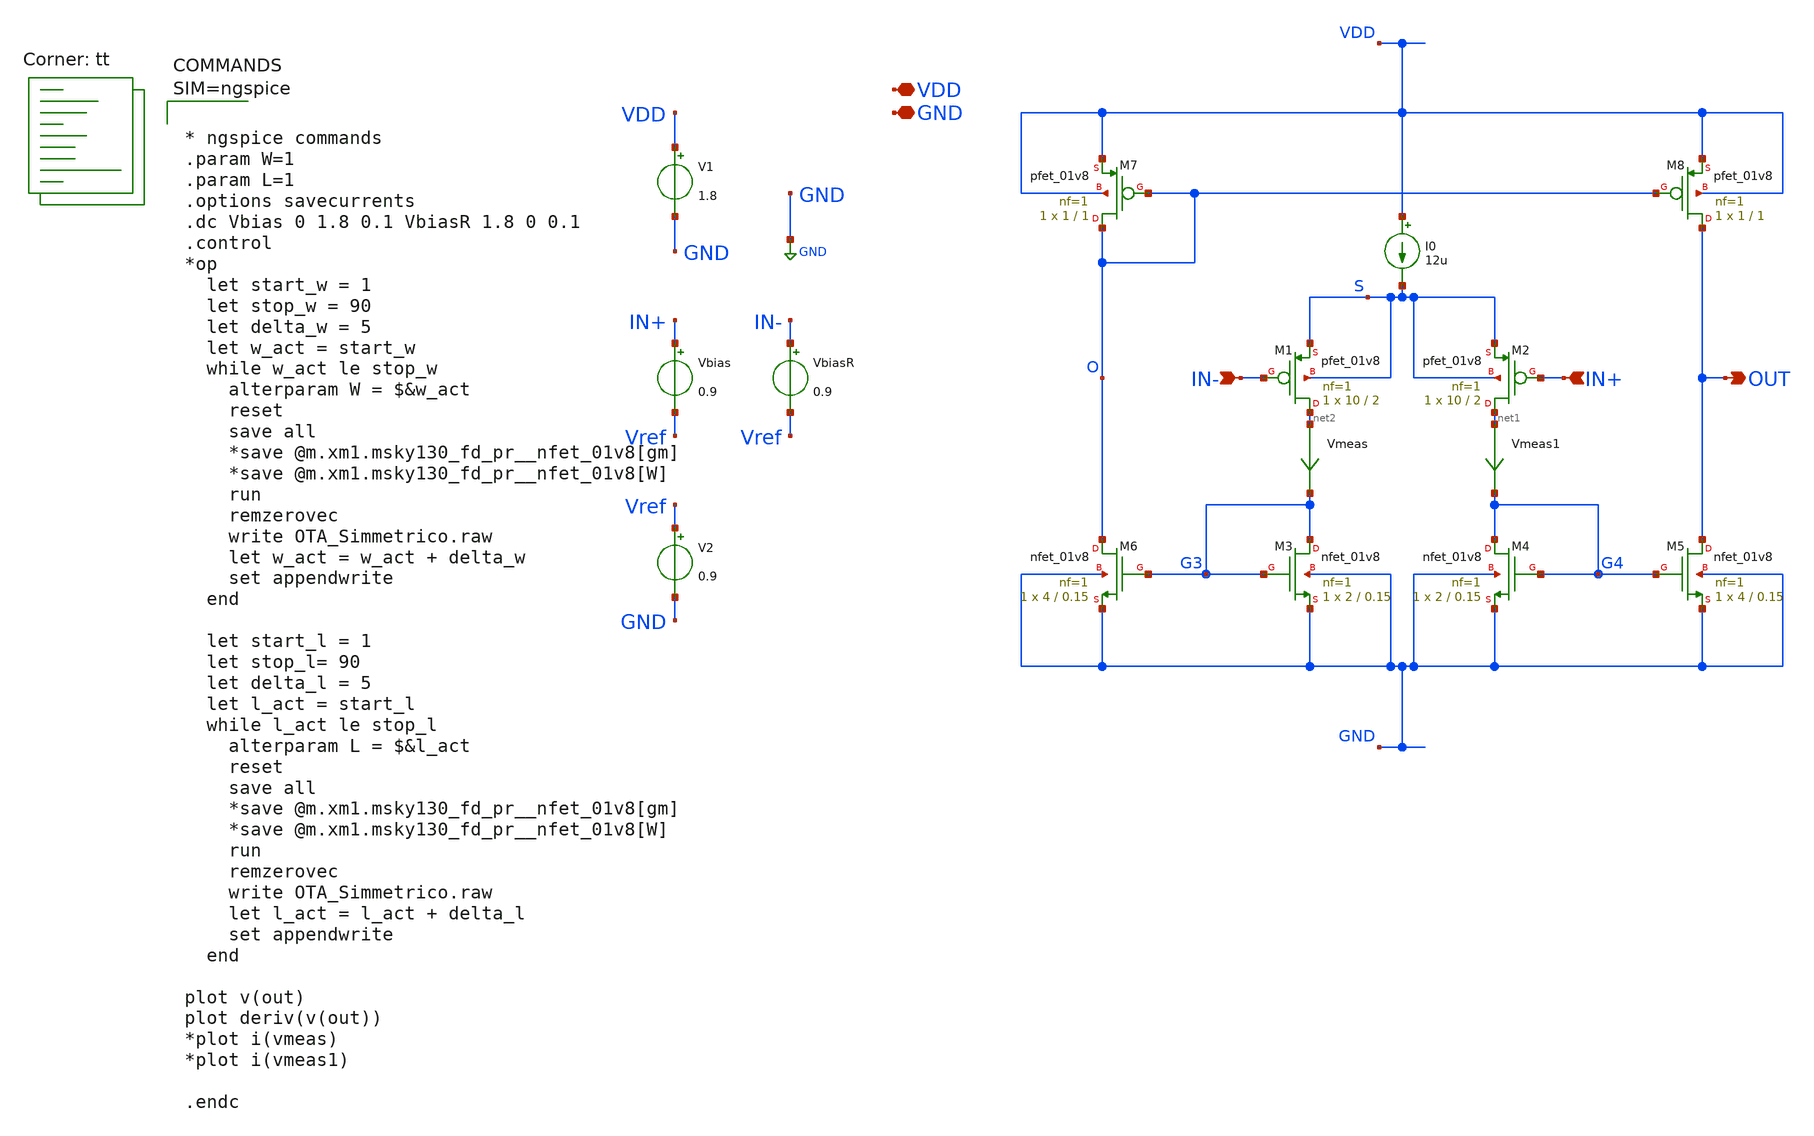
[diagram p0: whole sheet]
** sch_path: xschem/OTA_Simmetrico.sch
**.subckt OTA_Simmetrico VDD GND IN+ IN- OUT
*.iopin VDD
*.iopin GND
*.ipin IN+
*.ipin IN-
*.opin OUT
XM1 net2 IN- S S sky130_fd_pr__pfet_01v8 L=2 W=10 nf=1 ad='int((nf+1)/2) * W/nf * 0.29' as='int((nf+2)/2) * W/nf * 0.29'
+ pd='2*int((nf+1)/2) * (W/nf + 0.29)' ps='2*int((nf+2)/2) * (W/nf + 0.29)' nrd='0.29 / W' nrs='0.29 / W'
+ sa=0 sb=0 sd=0 mult=1 m=1
XM2 net1 IN+ S S sky130_fd_pr__pfet_01v8 L=2 W=10 nf=1 ad='int((nf+1)/2) * W/nf * 0.29' as='int((nf+2)/2) * W/nf * 0.29'
+ pd='2*int((nf+1)/2) * (W/nf + 0.29)' ps='2*int((nf+2)/2) * (W/nf + 0.29)' nrd='0.29 / W' nrs='0.29 / W'
+ sa=0 sb=0 sd=0 mult=1 m=1
XM3 G3 G3 GND GND sky130_fd_pr__nfet_01v8 L=0.15 W=2 nf=1 ad='int((nf+1)/2) * W/nf * 0.29' as='int((nf+2)/2) * W/nf * 0.29'
+ pd='2*int((nf+1)/2) * (W/nf + 0.29)' ps='2*int((nf+2)/2) * (W/nf + 0.29)' nrd='0.29 / W' nrs='0.29 / W'
+ sa=0 sb=0 sd=0 mult=1 m=1
XM4 G4 G4 GND GND sky130_fd_pr__nfet_01v8 L=0.15 W=2 nf=1 ad='int((nf+1)/2) * W/nf * 0.29' as='int((nf+2)/2) * W/nf * 0.29'
+ pd='2*int((nf+1)/2) * (W/nf + 0.29)' ps='2*int((nf+2)/2) * (W/nf + 0.29)' nrd='0.29 / W' nrs='0.29 / W'
+ sa=0 sb=0 sd=0 mult=1 m=1
XM5 OUT G4 GND GND sky130_fd_pr__nfet_01v8 L=0.15 W=4 nf=1 ad='int((nf+1)/2) * W/nf * 0.29' as='int((nf+2)/2) * W/nf * 0.29'
+ pd='2*int((nf+1)/2) * (W/nf + 0.29)' ps='2*int((nf+2)/2) * (W/nf + 0.29)' nrd='0.29 / W' nrs='0.29 / W'
+ sa=0 sb=0 sd=0 mult=1 m=1
XM6 O G3 GND GND sky130_fd_pr__nfet_01v8 L=0.15 W=4 nf=1 ad='int((nf+1)/2) * W/nf * 0.29' as='int((nf+2)/2) * W/nf * 0.29'
+ pd='2*int((nf+1)/2) * (W/nf + 0.29)' ps='2*int((nf+2)/2) * (W/nf + 0.29)' nrd='0.29 / W' nrs='0.29 / W'
+ sa=0 sb=0 sd=0 mult=1 m=1
XM7 O O VDD VDD sky130_fd_pr__pfet_01v8 L=1 W=1 nf=1 ad='int((nf+1)/2) * W/nf * 0.29' as='int((nf+2)/2) * W/nf * 0.29'
+ pd='2*int((nf+1)/2) * (W/nf + 0.29)' ps='2*int((nf+2)/2) * (W/nf + 0.29)' nrd='0.29 / W' nrs='0.29 / W'
+ sa=0 sb=0 sd=0 mult=1 m=1
XM8 OUT O VDD VDD sky130_fd_pr__pfet_01v8 L=1 W=1 nf=1 ad='int((nf+1)/2) * W/nf * 0.29' as='int((nf+2)/2) * W/nf * 0.29'
+ pd='2*int((nf+1)/2) * (W/nf + 0.29)' ps='2*int((nf+2)/2) * (W/nf + 0.29)' nrd='0.29 / W' nrs='0.29 / W'
+ sa=0 sb=0 sd=0 mult=1 m=1
I0 VDD S 12u
V1 VDD GND 1.8
Vbias IN+ Vref 0.9
VbiasR IN- Vref 0.9
V2 Vref GND 0.9
Vmeas net2 G3 0
.save i(vmeas)
Vmeas1 net1 G4 0
.save i(vmeas1)
**** begin user architecture code



* ngspice commands
.param W=1
.param L=1
.options savecurrents
.dc Vbias 0 1.8 0.1 VbiasR 1.8 0 0.1
.control
*op
  let start_w = 1
  let stop_w = 90
  let delta_w = 5
  let w_act = start_w
  while w_act le stop_w
    alterparam W = $&w_act
    reset
    save all
    *save @m.xm1.msky130_fd_pr__nfet_01v8[gm]
    *save @m.xm1.msky130_fd_pr__nfet_01v8[W]
    run
    remzerovec
    write OTA_Simmetrico.raw
    let w_act = w_act + delta_w
    set appendwrite
  end

  let start_l = 1
  let stop_l= 90
  let delta_l = 5
  let l_act = start_l
  while l_act le stop_l
    alterparam L = $&l_act
    reset
    save all
    *save @m.xm1.msky130_fd_pr__nfet_01v8[gm]
    *save @m.xm1.msky130_fd_pr__nfet_01v8[W]
    run
    remzerovec
    write OTA_Simmetrico.raw
    let l_act = l_act + delta_l
    set appendwrite
  end

plot v(out)
plot deriv(v(out))
*plot i(vmeas)
*plot i(vmeas1)

.endc



.lib $::SKYWATER_MODELS/sky130.lib.spice tt
**** end user architecture code
**.ends
.GLOBAL GND
.end
